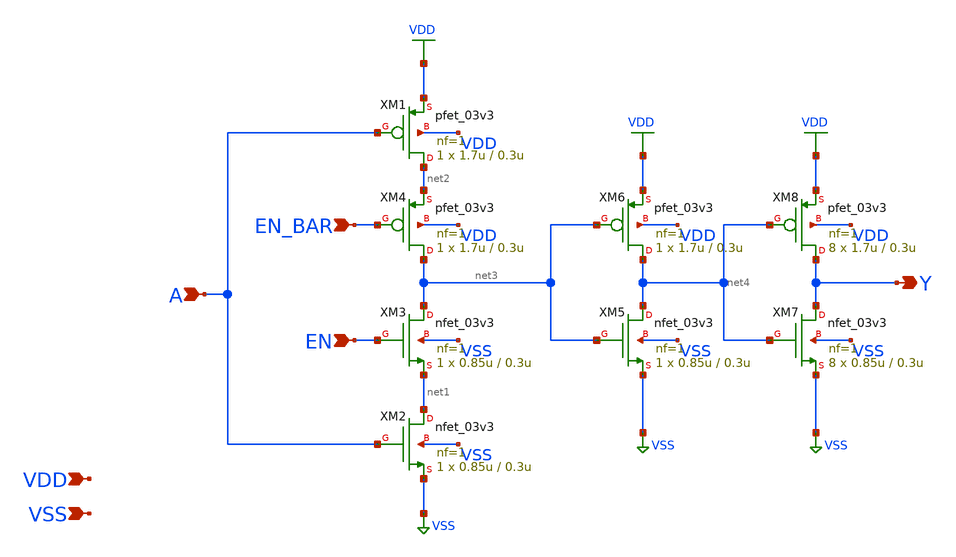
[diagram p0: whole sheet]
** sch_path: gf180mcu_osu_sc_gp12t3v3/xschem/gf180mcu_osu_sc_gp12t3v3__tinv_8.sch
**.subckt gf180mcu_osu_sc_gp12t3v3__tinv_8 A EN EN_BAR Y VDD VSS
*.ipin A
*.ipin EN
*.ipin EN_BAR
*.opin Y
*.ipin VDD
*.ipin VSS
XM1 net2 A VDD VDD pfet_03v3 L=0.3u W=1.7u nf=1 ad='int((nf+1)/2) * W/nf * 0.18u' as='int((nf+2)/2) * W/nf * 0.18u'
+ pd='2*int((nf+1)/2) * (W/nf + 0.18u)' ps='2*int((nf+2)/2) * (W/nf + 0.18u)' nrd='0.18u / W' nrs='0.18u / W'
+ sa=0 sb=0 sd=0 m=1
XM2 net1 A VSS VSS nfet_03v3 L=0.3u W=0.85u nf=1 ad='int((nf+1)/2) * W/nf * 0.18u' as='int((nf+2)/2) * W/nf * 0.18u'
+ pd='2*int((nf+1)/2) * (W/nf + 0.18u)' ps='2*int((nf+2)/2) * (W/nf + 0.18u)' nrd='0.18u / W' nrs='0.18u / W'
+ sa=0 sb=0 sd=0 m=1
XM3 net3 EN net1 VSS nfet_03v3 L=0.3u W=0.85u nf=1 ad='int((nf+1)/2) * W/nf * 0.18u' as='int((nf+2)/2) * W/nf * 0.18u'
+ pd='2*int((nf+1)/2) * (W/nf + 0.18u)' ps='2*int((nf+2)/2) * (W/nf + 0.18u)' nrd='0.18u / W' nrs='0.18u / W'
+ sa=0 sb=0 sd=0 m=1
XM4 net3 EN_BAR net2 VDD pfet_03v3 L=0.3u W=1.7u nf=1 ad='int((nf+1)/2) * W/nf * 0.18u' as='int((nf+2)/2) * W/nf * 0.18u'
+ pd='2*int((nf+1)/2) * (W/nf + 0.18u)' ps='2*int((nf+2)/2) * (W/nf + 0.18u)' nrd='0.18u / W' nrs='0.18u / W'
+ sa=0 sb=0 sd=0 m=1
XM5 net4 net3 VSS VSS nfet_03v3 L=0.3u W=0.85u nf=1 ad='int((nf+1)/2) * W/nf * 0.18u' as='int((nf+2)/2) * W/nf * 0.18u'
+ pd='2*int((nf+1)/2) * (W/nf + 0.18u)' ps='2*int((nf+2)/2) * (W/nf + 0.18u)' nrd='0.18u / W' nrs='0.18u / W'
+ sa=0 sb=0 sd=0 m=1
XM6 net4 net3 VDD VDD pfet_03v3 L=0.3u W=1.7u nf=1 ad='int((nf+1)/2) * W/nf * 0.18u' as='int((nf+2)/2) * W/nf * 0.18u'
+ pd='2*int((nf+1)/2) * (W/nf + 0.18u)' ps='2*int((nf+2)/2) * (W/nf + 0.18u)' nrd='0.18u / W' nrs='0.18u / W'
+ sa=0 sb=0 sd=0 m=1
XM7 Y net4 VSS VSS nfet_03v3 L=0.3u W=0.85u nf=1 ad='int((nf+1)/2) * W/nf * 0.18u' as='int((nf+2)/2) * W/nf * 0.18u'
+ pd='2*int((nf+1)/2) * (W/nf + 0.18u)' ps='2*int((nf+2)/2) * (W/nf + 0.18u)' nrd='0.18u / W' nrs='0.18u / W'
+ sa=0 sb=0 sd=0 m=8
XM8 Y net4 VDD VDD pfet_03v3 L=0.3u W=1.7u nf=1 ad='int((nf+1)/2) * W/nf * 0.18u' as='int((nf+2)/2) * W/nf * 0.18u'
+ pd='2*int((nf+1)/2) * (W/nf + 0.18u)' ps='2*int((nf+2)/2) * (W/nf + 0.18u)' nrd='0.18u / W' nrs='0.18u / W'
+ sa=0 sb=0 sd=0 m=8
**.ends
.GLOBAL VDD
.GLOBAL VSS
.end
